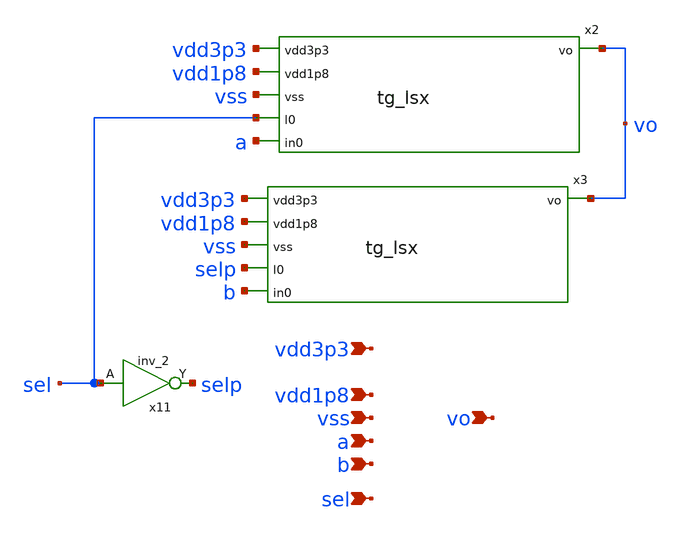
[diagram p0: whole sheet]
** sch_path: spice/xschem/EF_AMUX21x.sch
**.subckt EF_AMUX21x vdd1p8 vss a b vdd3p3 sel vo
*.ipin vdd1p8
*.ipin vss
*.ipin a
*.ipin b
*.ipin vdd3p3
*.ipin sel
*.ipin vo
x2 vdd3p3 vdd1p8 vss sel vo a tg_lsx
x3 vdd3p3 vdd1p8 vss selp vo b tg_lsx
x11 sel vss vss vdd1p8 vdd1p8 selp sky130_fd_sc_hvl__inv_2
**.ends
.end
